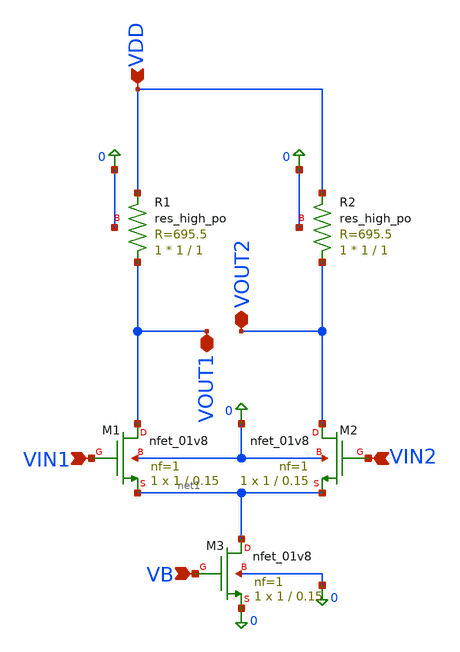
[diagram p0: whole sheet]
** sch_path: MOS-Circuits/Differential Pair/Diff_pair Basics/diff_pair.sch
**.subckt diff_pair VIN1 VIN2 VB VDD VOUT1 VOUT2
*.ipin VIN1
*.ipin VIN2
*.ipin VB
*.ipin VDD
*.iopin VOUT1
*.iopin VOUT2
XM1 VOUT1 VIN1 net1 0 sky130_fd_pr__nfet_01v8 L=0.15 W=1 nf=1 ad='int((nf+1)/2) * W/nf * 0.29' as='int((nf+2)/2) * W/nf * 0.29'
+ pd='2*int((nf+1)/2) * (W/nf + 0.29)' ps='2*int((nf+2)/2) * (W/nf + 0.29)' nrd='0.29 / W' nrs='0.29 / W'
+ sa=0 sb=0 sd=0 mult=1 m=1
XM2 VOUT2 VIN2 net1 0 sky130_fd_pr__nfet_01v8 L=0.15 W=1 nf=1 ad='int((nf+1)/2) * W/nf * 0.29' as='int((nf+2)/2) * W/nf * 0.29'
+ pd='2*int((nf+1)/2) * (W/nf + 0.29)' ps='2*int((nf+2)/2) * (W/nf + 0.29)' nrd='0.29 / W' nrs='0.29 / W'
+ sa=0 sb=0 sd=0 mult=1 m=1
XM3 net1 VB 0 0 sky130_fd_pr__nfet_01v8 L=0.15 W=1 nf=1 ad='int((nf+1)/2) * W/nf * 0.29' as='int((nf+2)/2) * W/nf * 0.29'
+ pd='2*int((nf+1)/2) * (W/nf + 0.29)' ps='2*int((nf+2)/2) * (W/nf + 0.29)' nrd='0.29 / W' nrs='0.29 / W'
+ sa=0 sb=0 sd=0 mult=1 m=1
XR1 VOUT1 VDD 0 sky130_fd_pr__res_high_po W=1 L=1 mult=1 m=1
XR2 VOUT2 VDD 0 sky130_fd_pr__res_high_po W=1 L=1 mult=1 m=1
**.ends
.end
